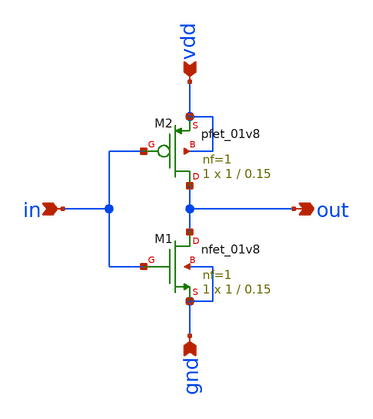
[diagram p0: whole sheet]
** sch_path: xschem/attenuator/basic-invert.sch
**.subckt basic-invert in gnd vdd out
*.ipin in
*.ipin gnd
*.ipin vdd
*.opin out
XM1 out in gnd gnd sky130_fd_pr__nfet_01v8 L=0.15 W=1 nf=1 ad='int((nf+1)/2) * W/nf * 0.29' as='int((nf+2)/2) * W/nf * 0.29'
+ pd='2*int((nf+1)/2) * (W/nf + 0.29)' ps='2*int((nf+2)/2) * (W/nf + 0.29)' nrd='0.29 / W' nrs='0.29 / W'
+ sa=0 sb=0 sd=0 mult=1 m=1
XM2 out in vdd vdd sky130_fd_pr__pfet_01v8 L=0.15 W=1 nf=1 ad='int((nf+1)/2) * W/nf * 0.29' as='int((nf+2)/2) * W/nf * 0.29'
+ pd='2*int((nf+1)/2) * (W/nf + 0.29)' ps='2*int((nf+2)/2) * (W/nf + 0.29)' nrd='0.29 / W' nrs='0.29 / W'
+ sa=0 sb=0 sd=0 mult=1 m=1
**** begin user architecture code
 ** manual skywater pdks install (with patches applied)
* .lib $::SKYWATER_MODELS/models/sky130.lib.spice tt
*** remove the /models/

** opencircuitdesign pdks install
.lib /Volumes/WORK_DRIVE/open_pdks/sky130/custom/models/sky130.lib.spice tt

.param mc_mm_switch=0
.param mc_pr_switch=0

**** end user architecture code
**.ends
.end
